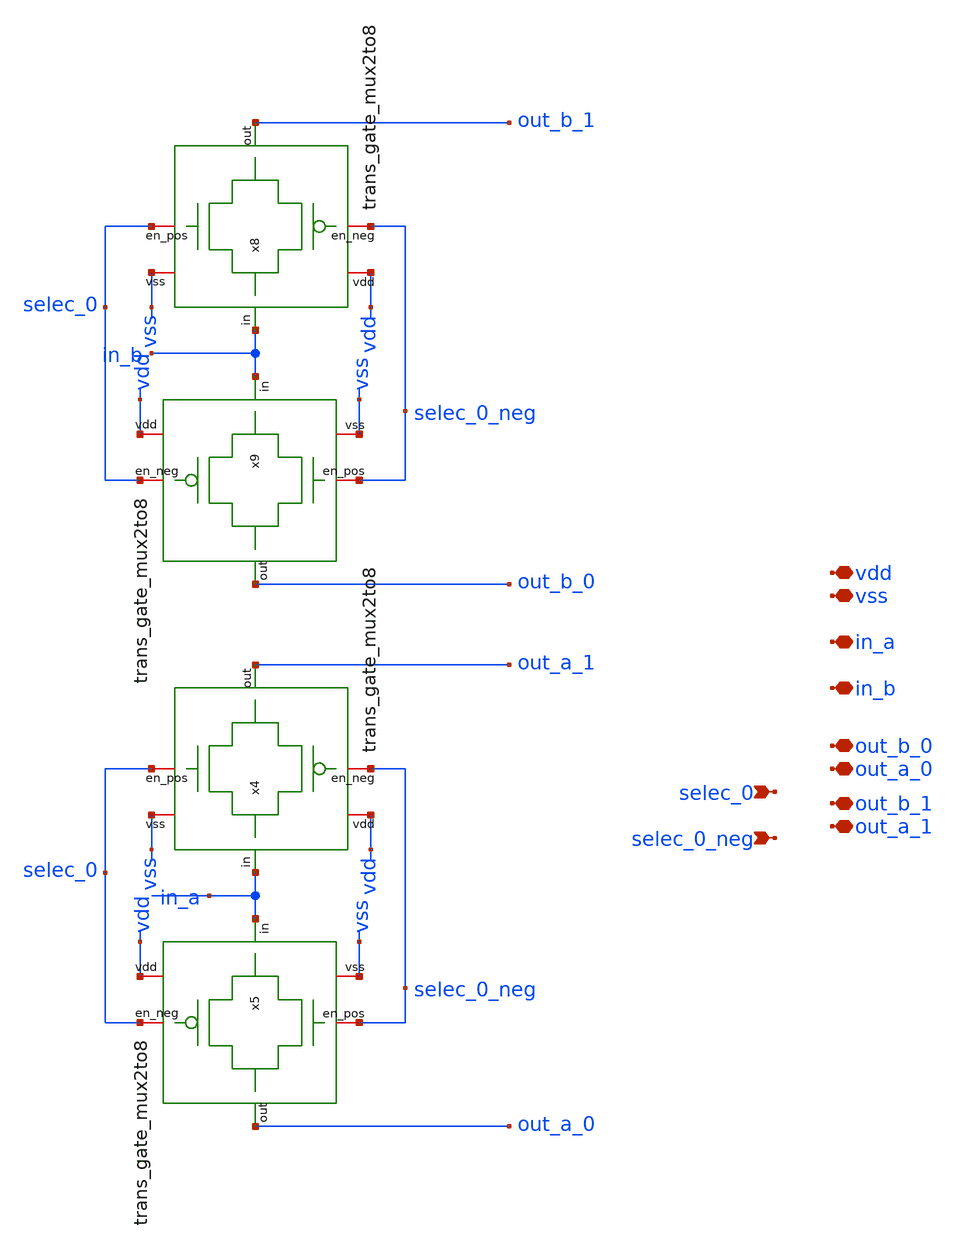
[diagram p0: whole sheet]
** sch_path: xschem/mux2to4.sch
**.subckt mux2to4 in_a in_b selec_0_neg selec_0 out_b_0 out_b_1 out_a_0 out_a_1 vdd vss
*.iopin in_a
*.iopin in_b
*.ipin selec_0_neg
*.ipin selec_0
*.iopin out_b_0
*.iopin out_b_1
*.iopin out_a_0
*.iopin out_a_1
*.iopin vdd
*.iopin vss
x4 selec_0 out_a_1 in_a selec_0_neg vss vdd trans_gate_mux2to8
x5 selec_0_neg out_a_0 in_a selec_0 vss vdd trans_gate_mux2to8
x8 selec_0 out_b_1 in_b selec_0_neg vss vdd trans_gate_mux2to8
x9 selec_0_neg out_b_0 in_b selec_0 vss vdd trans_gate_mux2to8
**.ends

* expanding   symbol:  trans_gate_mux2to8.sym # of pins=6
** sym_path: xschem/trans_gate_mux2to8.sym
** sch_path: xschem/trans_gate_mux2to8.sch
.subckt trans_gate_mux2to8 en_pos out in en_neg vss vdd
*.iopin en_neg
*.ipin in
*.opin out
*.iopin en_pos
*.iopin vdd
*.iopin vss
XM2 out en_neg in vdd sky130_fd_pr__pfet_01v8 L=0.15 W=1.25 nf=1 ad='int((nf+1)/2) * W/nf * 0.29' as='int((nf+2)/2) * W/nf * 0.29'
+ pd='2*int((nf+1)/2) * (W/nf + 0.29)' ps='2*int((nf+2)/2) * (W/nf + 0.29)' nrd='0.29 / W' nrs='0.29 / W'
+ sa=0 sb=0 sd=0 mult=3 m=3
XM1 out en_pos in vss sky130_fd_pr__nfet_01v8 L=0.15 W=1.25 nf=1 ad='int((nf+1)/2) * W/nf * 0.29' as='int((nf+2)/2) * W/nf * 0.29'
+ pd='2*int((nf+1)/2) * (W/nf + 0.29)' ps='2*int((nf+2)/2) * (W/nf + 0.29)' nrd='0.29 / W' nrs='0.29 / W'
+ sa=0 sb=0 sd=0 mult=3 m=3
.ends

.end
